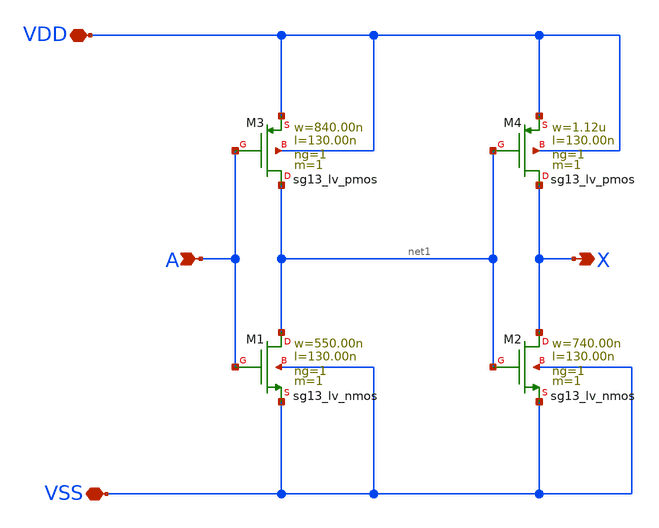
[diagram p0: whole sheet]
** sch_path: ihp-sg13g2/libs.tech/xschem/sg13g2_stdcells/sg13g2_buf_1.sch
* Copyright 2023 IHP PDK Authors
* Licensed under the Apache License, Version 2.0 (the "License");
* you may not use this file except in compliance with the License.
* You may obtain a copy of the License at
* https://www.apache.org/licenses/LICENSE-2.0
* Unless required by applicable law or agreed to in writing, software
* distributed under the License is distributed on an "AS IS" BASIS,
* WITHOUT WARRANTIES OR CONDITIONS OF ANY KIND, either express or implied.
* See the License for the specific language governing permissions and
* limitations under the License.
**.subckt sg13g2_buf_1 A X VDD VSS
*.ipin A
*.opin X
*.iopin VDD
*.iopin VSS
XM1 net1 A VSS VSS sg13_lv_nmos w=550.00n l=130.00n ng=1 m=1 mm_ok=1
XM2 X net1 VSS VSS sg13_lv_nmos w=740.00n l=130.00n ng=1 m=1 mm_ok=1
XM3 net1 A VDD VDD sg13_lv_pmos w=840.00n l=130.00n ng=1 m=1 mm_ok=1
XM4 X net1 VDD VDD sg13_lv_pmos w=1.12u l=130.00n ng=1 m=1 mm_ok=1
**.ends
.end
